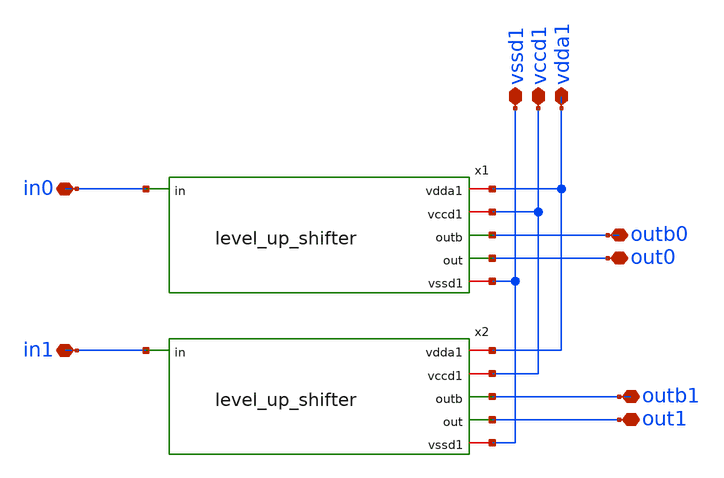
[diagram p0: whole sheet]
** sch_path: xschem/tryandtest/level_up_shifter_test.sch
**.subckt level_up_shifter_test vssd1 vccd1 vdda1 in0 in1 outb0 outb1 out0 out1
*.iopin vssd1
*.iopin vccd1
*.iopin vdda1
*.iopin in0
*.iopin in1
*.iopin outb0
*.iopin outb1
*.iopin out0
*.iopin out1
x1 vdda1 vccd1 in0 outb0 out0 vssd1 level_up_shifter
x2 vdda1 vccd1 in1 outb1 out1 vssd1 level_up_shifter
**.ends
.end
